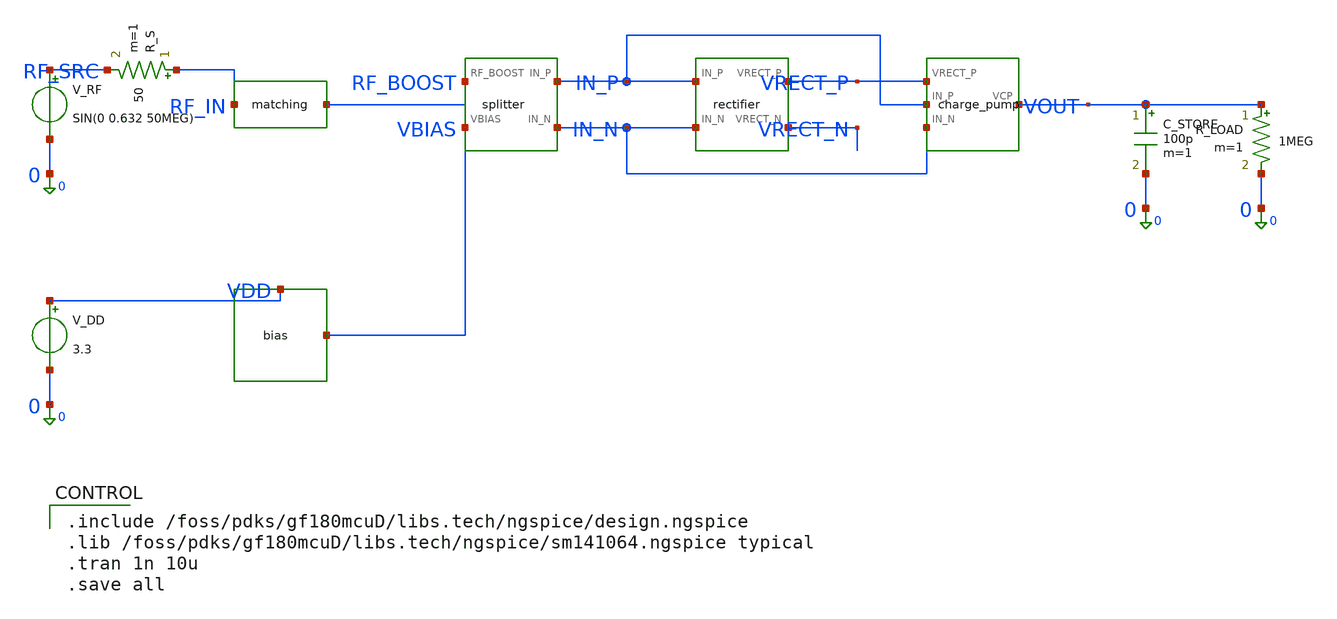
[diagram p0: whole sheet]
** sch_path: modules/PandaChip/designs/iris-harvester/tb_iris.sch
**.subckt tb_iris
X1 RF_IN RF_BOOST matching
X2 VDD VBIAS bias
X3 RF_BOOST VBIAS IN_P IN_N splitter
X4 IN_P IN_N VRECT_P VRECT_N rectifier
X5 VRECT_P IN_P IN_N VOUT charge_pump
V_RF RF_SRC 0 SIN(0 0.632 50MEG)
R_S RF_IN RF_SRC 50 m=1
V_DD VDD 0 3.3
C_STORE VOUT 0 100p m=1
R_LOAD VOUT 0 1MEG m=1
**** begin user architecture code

.include /foss/pdks/gf180mcuD/libs.tech/ngspice/design.ngspice
.lib /foss/pdks/gf180mcuD/libs.tech/ngspice/sm141064.ngspice typical
.tran 1n 10u
.save all

**** end user architecture code
**.ends

* expanding   symbol:  matching.sym # of pins=2
** sym_path: modules/PandaChip/designs/iris-harvester/matching.sym
** sch_path: modules/PandaChip/designs/iris-harvester/matching.sch
.subckt matching RF_IN RF_BOOST
*.iopin RF_IN
*.iopin RF_BOOST
L1 RF_BOOST RF_IN 694n m=1
C1 RF_BOOST 0 14p m=1
.ends


* expanding   symbol:  bias.sym # of pins=2
** sym_path: modules/PandaChip/designs/iris-harvester/bias.sym
** sch_path: modules/PandaChip/designs/iris-harvester/bias.sch
.subckt bias VDD VBIAS
*.iopin VDD
*.iopin VBIAS
I1 VDD VBIAS 1u
XM1 VBIAS VBIAS 0 0 nfet_03v3 L=0.28u W=10u nf=2 ad='int((nf+1)/2) * W/nf * 0.18u' as='int((nf+2)/2) * W/nf * 0.18u'
+ pd='2*int((nf+1)/2) * (W/nf + 0.18u)' ps='2*int((nf+2)/2) * (W/nf + 0.18u)' nrd='0.18u / W' nrs='0.18u / W'
+ sa=0 sb=0 sd=0 m=1
.ends


* expanding   symbol:  splitter.sym # of pins=4
** sym_path: modules/PandaChip/designs/iris-harvester/splitter.sym
** sch_path: modules/PandaChip/designs/iris-harvester/splitter.sch
.subckt splitter RF_BOOST VBIAS IN_P IN_N
*.iopin RF_BOOST
*.iopin VBIAS
*.iopin IN_P
*.iopin IN_N
C1 IN_P RF_P 10p m=1
C2 IN_N RF_N 10p m=1
R1 VBIAS IN_P 100k m=1
R2 IN_N VBIAS 100k m=1
**** begin user architecture code

E1 RF_P 0 RF_BOOST 0 1
E2 RF_N 0 RF_BOOST 0 -1

**** end user architecture code
.ends


* expanding   symbol:  rectifier.sym # of pins=4
** sym_path: modules/PandaChip/designs/iris-harvester/exp/rectifier.sym
** sch_path: modules/PandaChip/designs/iris-harvester/exp/rectifier.sch
.subckt rectifier IN_P IN_N VRECT_P VRECT_N
*.ipin IN_P
*.ipin IN_N
*.opin VRECT_P
*.opin VRECT_N
XM_P1 IN_P IN_N VRECT_P VRECT_P pfet_03v3 L=0.28u W=20u nf=2 ad='int((nf+1)/2) * W/nf * 0.18u' as='int((nf+2)/2) * W/nf * 0.18u'
+ pd='2*int((nf+1)/2) * (W/nf + 0.18u)' ps='2*int((nf+2)/2) * (W/nf + 0.18u)' nrd='0.18u / W' nrs='0.18u / W'
+ sa=0 sb=0 sd=0 m=1
XM_P2 IN_N IN_P VRECT_P VRECT_P pfet_03v3 L=0.28u W=20u nf=2 ad='int((nf+1)/2) * W/nf * 0.18u' as='int((nf+2)/2) * W/nf * 0.18u'
+ pd='2*int((nf+1)/2) * (W/nf + 0.18u)' ps='2*int((nf+2)/2) * (W/nf + 0.18u)' nrd='0.18u / W' nrs='0.18u / W'
+ sa=0 sb=0 sd=0 m=1
XM_N1 IN_P IN_N VRECT_N VRECT_N nfet_03v3 L=0.28u W=20u nf=2 ad='int((nf+1)/2) * W/nf * 0.18u' as='int((nf+2)/2) * W/nf * 0.18u'
+ pd='2*int((nf+1)/2) * (W/nf + 0.18u)' ps='2*int((nf+2)/2) * (W/nf + 0.18u)' nrd='0.18u / W' nrs='0.18u / W'
+ sa=0 sb=0 sd=0 m=1
XM_N2 IN_N IN_P VRECT_N VRECT_N nfet_03v3 L=0.28u W=20u nf=2 ad='int((nf+1)/2) * W/nf * 0.18u' as='int((nf+2)/2) * W/nf * 0.18u'
+ pd='2*int((nf+1)/2) * (W/nf + 0.18u)' ps='2*int((nf+2)/2) * (W/nf + 0.18u)' nrd='0.18u / W' nrs='0.18u / W'
+ sa=0 sb=0 sd=0 m=1
XM_D1 0 0 VRECT_N 0 nfet_03v3 L=0.28u W=10u nf=2 ad='int((nf+1)/2) * W/nf * 0.18u' as='int((nf+2)/2) * W/nf * 0.18u'
+ pd='2*int((nf+1)/2) * (W/nf + 0.18u)' ps='2*int((nf+2)/2) * (W/nf + 0.18u)' nrd='0.18u / W' nrs='0.18u / W'
+ sa=0 sb=0 sd=0 m=1
V_DUMMY1 VRECT_P DUMMY_NET1 0
V_DUMMY2 VRECT_N DUMMY_NET2 0
.ends


* expanding   symbol:  charge_pump.sym # of pins=4
** sym_path: modules/PandaChip/designs/iris-harvester/exp/charge_pump.sym
** sch_path: modules/PandaChip/designs/iris-harvester/exp/charge_pump.sch
.subckt charge_pump VRECT_P IN_P IN_N VCP
*.ipin VRECT_P
*.ipin IN_N
*.ipin IN_P
*.opin VCP
XM_D1 VRECT_P VRECT_P N1 0 nfet_03v3 L=0.28u W=10u nf=2 ad='int((nf+1)/2) * W/nf * 0.18u' as='int((nf+2)/2) * W/nf * 0.18u'
+ pd='2*int((nf+1)/2) * (W/nf + 0.18u)' ps='2*int((nf+2)/2) * (W/nf + 0.18u)' nrd='0.18u / W' nrs='0.18u / W'
+ sa=0 sb=0 sd=0 m=1
XM_D2 N1 N1 N2 0 nfet_03v3 L=0.28u W=10u nf=2 ad='int((nf+1)/2) * W/nf * 0.18u' as='int((nf+2)/2) * W/nf * 0.18u'
+ pd='2*int((nf+1)/2) * (W/nf + 0.18u)' ps='2*int((nf+2)/2) * (W/nf + 0.18u)' nrd='0.18u / W' nrs='0.18u / W'
+ sa=0 sb=0 sd=0 m=1
XM_D3 N2 N2 N3 0 nfet_03v3 L=0.28u W=10u nf=2 ad='int((nf+1)/2) * W/nf * 0.18u' as='int((nf+2)/2) * W/nf * 0.18u'
+ pd='2*int((nf+1)/2) * (W/nf + 0.18u)' ps='2*int((nf+2)/2) * (W/nf + 0.18u)' nrd='0.18u / W' nrs='0.18u / W'
+ sa=0 sb=0 sd=0 m=1
XM_D4 N3 N3 VCP 0 nfet_03v3 L=0.28u W=10u nf=2 ad='int((nf+1)/2) * W/nf * 0.18u' as='int((nf+2)/2) * W/nf * 0.18u'
+ pd='2*int((nf+1)/2) * (W/nf + 0.18u)' ps='2*int((nf+2)/2) * (W/nf + 0.18u)' nrd='0.18u / W' nrs='0.18u / W'
+ sa=0 sb=0 sd=0 m=1
C1 N1 IN_N 10p m=1
C2 N2 IN_P 10p m=1
C3 N3 IN_N 10p m=1
R_DUMMY1 VCP 0 1T m=1
.ends

.end
